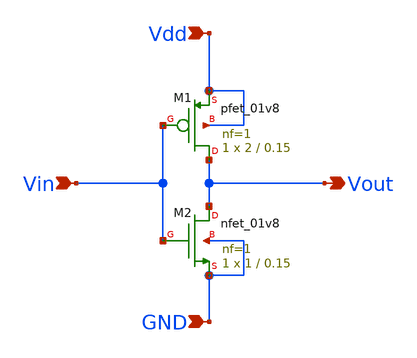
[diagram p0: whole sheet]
** sch_path: inverter.sch
**.subckt inverter Vin Vdd GND Vout
*.ipin Vin
*.ipin Vdd
*.ipin GND
*.opin Vout
XM2 Vout Vin GND GND sky130_fd_pr__nfet_01v8 L=0.15 W=1 nf=1 ad='int((1 + 1)/2) * 1 / 1 * 0.29' as='int((1 + 2)/2) * 1 / 1 * 0.29'
+ pd='2*int((1 + 1)/2) * (1 / 1 + 0.29)' ps='2*int((1 + 2)/2) * (1 / 1 + 0.29)' nrd='0.29 / 1 ' nrs='0.29 / 1 '
+ sa=0 sb=0 sd=0 mult=1 m=1
XM1 Vout Vin Vdd Vdd sky130_fd_pr__pfet_01v8 L=0.15 W=2 nf=1 ad='int((1 + 1)/2) * 2 / 1 * 0.29' as='int((1 + 2)/2) * 2 / 1 * 0.29'
+ pd='2*int((1 + 1)/2) * (2 / 1 + 0.29)' ps='2*int((1 + 2)/2) * (2 / 1 + 0.29)' nrd='0.29 / 2 ' nrs='0.29 / 2 '
+ sa=0 sb=0 sd=0 mult=1 m=1
**.ends
.end
